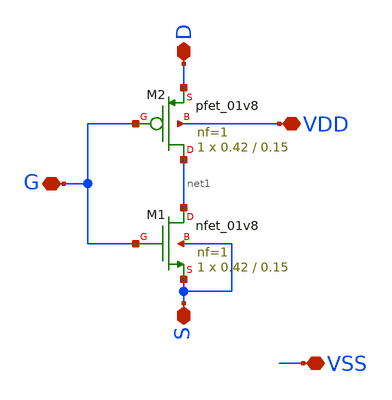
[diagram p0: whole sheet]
** sch_path: sky130A/schematic/xschem/sky130_dnwell_inv.sch
**.subckt sky130_dnwell_inv S VSS D G VDD
*.iopin S
*.iopin VSS
*.iopin D
*.iopin G
*.iopin VDD
XM1 net1 G S S sky130_fd_pr__nfet_01v8 L=0.15 W=0.42 nf=1 ad='int((1 + 1)/2) * 0.42 / 1 * 0.29' as='int((1 + 2)/2) * 0.42 / 1 * 0.29'
+ pd='2*int((1 + 1)/2) * (0.42 / 1 + 0.29)' ps='2*int((1 + 2)/2) * (0.42 / 1 + 0.29)' nrd='0.29 / 0.42 '
+ nrs='0.29 / 0.42 ' sa=0 sb=0 sd=0 mult=1 m=1
XM2 net1 G D VDD sky130_fd_pr__pfet_01v8 L=0.15 W=0.42 nf=1 ad='int((1 + 1)/2) * 0.42 / 1 * 0.29' as='int((1 + 2)/2) * 0.42 / 1 * 0.29'
+ pd='2*int((1 + 1)/2) * (0.42 / 1 + 0.29)' ps='2*int((1 + 2)/2) * (0.42 / 1 + 0.29)' nrd='0.29 / 0.42 '
+ nrs='0.29 / 0.42 ' sa=0 sb=0 sd=0 mult=1 m=1
**.ends
.end
